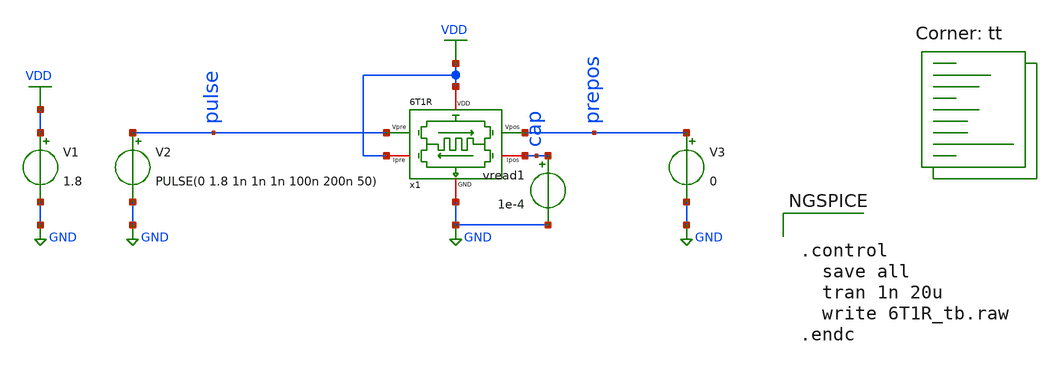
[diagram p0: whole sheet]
** sch_path: synapse/6T1R_tb.sch
**.subckt 6T1R_tb
V2 pulse GND PULSE(0 1.8 1n 1n 1n 100n 200n 50)
V1 VDD GND 1.8
V3 prepos GND 0
x1 VDD VDD cap pulse prepos GND 6T1R
vread1 cap GND 1e-4
**** begin user architecture code
.lib $::SKYWATER_MODELS/sky130.lib.spice tt

** opencircuitdesign pdks install
.inc $::SKYWATER_MODELS/rram_v0.spice



.control
  save all
  tran 1n 20u
  write 6T1R_tb.raw
.endc


**** end user architecture code
**.ends

* expanding   symbol:  /home/ricardo/RATT_repos/Proyectos_xschem/synapse/6T1R.sym # of pins=6
** sym_path: synapse/6T1R.sym
** sch_path: synapse/6T1R.sch
.subckt 6T1R Ipre VDD Ipos Vpre Vpos GND
*.ipin Vpre
*.ipin Vpos
*.iopin GND
*.iopin Ipos
*.iopin Ipre
*.iopin VDD
XM1 BE Vpre vipre GND sky130_fd_pr__nfet_01v8 L=0.15 W=15 nf=1 ad='int((nf+1)/2) * W/nf * 0.29' as='int((nf+2)/2) * W/nf * 0.29'
+ pd='2*int((nf+1)/2) * (W/nf + 0.29)' ps='2*int((nf+2)/2) * (W/nf + 0.29)' nrd='0.29 / W' nrs='0.29 / W'
+ sa=0 sb=0 sd=0 mult=1 m=1
XR1 TE BE rram_v0
XM3 TE Vpos vipre GND sky130_fd_pr__nfet_01v8 L=0.15 W=15 nf=1 ad='int((nf+1)/2) * W/nf * 0.29' as='int((nf+2)/2) * W/nf * 0.29'
+ pd='2*int((nf+1)/2) * (W/nf + 0.29)' ps='2*int((nf+2)/2) * (W/nf + 0.29)' nrd='0.29 / W' nrs='0.29 / W'
+ sa=0 sb=0 sd=0 mult=1 m=1
XM6 Ipos vipre VDD VDD sky130_fd_pr__pfet_01v8 L=0.15 W=20 nf=1 ad='int((nf+1)/2) * W/nf * 0.29' as='int((nf+2)/2) * W/nf * 0.29'
+ pd='2*int((nf+1)/2) * (W/nf + 0.29)' ps='2*int((nf+2)/2) * (W/nf + 0.29)' nrd='0.29 / W' nrs='0.29 / W'
+ sa=0 sb=0 sd=0 mult=1 m=1
XM5 vipre vipre Ipre VDD sky130_fd_pr__pfet_01v8 L=0.15 W=20 nf=1 ad='int((nf+1)/2) * W/nf * 0.29' as='int((nf+2)/2) * W/nf * 0.29'
+ pd='2*int((nf+1)/2) * (W/nf + 0.29)' ps='2*int((nf+2)/2) * (W/nf + 0.29)' nrd='0.29 / W' nrs='0.29 / W'
+ sa=0 sb=0 sd=0 mult=1 m=1
XM2 GND Vpos BE GND sky130_fd_pr__nfet_01v8 L=0.15 W=15 nf=1 ad='int((nf+1)/2) * W/nf * 0.29' as='int((nf+2)/2) * W/nf * 0.29'
+ pd='2*int((nf+1)/2) * (W/nf + 0.29)' ps='2*int((nf+2)/2) * (W/nf + 0.29)' nrd='0.29 / W' nrs='0.29 / W'
+ sa=0 sb=0 sd=0 mult=1 m=1
XM4 GND Vpre TE GND sky130_fd_pr__nfet_01v8 L=0.15 W=15 nf=1 ad='int((nf+1)/2) * W/nf * 0.29' as='int((nf+2)/2) * W/nf * 0.29'
+ pd='2*int((nf+1)/2) * (W/nf + 0.29)' ps='2*int((nf+2)/2) * (W/nf + 0.29)' nrd='0.29 / W' nrs='0.29 / W'
+ sa=0 sb=0 sd=0 mult=1 m=1
.ends

.GLOBAL GND
.GLOBAL VDD
.end
